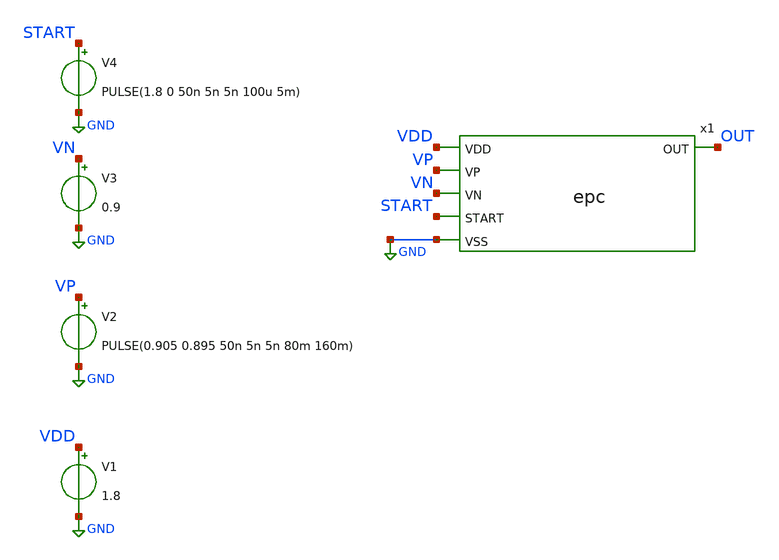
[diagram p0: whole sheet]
** sch_path: xschem/epc_tb.sch
**.subckt epc_tb
x1 VDD VP OUT VN START GND epc
V1 VDD GND 1.8
V2 VP GND PULSE(0.905 0.895 50n 5n 5n 80m 160m)
V3 VN GND 0.9
V4 START GND PULSE(1.8 0 50n 5n 5n 100u 5m)
**** begin user architecture code

** opencircuitdesign pdks install
.lib $::SKYWATER_MODELS/sky130.lib.spice tt
.include /usr/local/share/pdk/sky130A/libs.ref/sky130_fd_sc_hd/spice/sky130_fd_sc_hd.spice



.option wnflag=0
.option savecurrents
.control
tran 1m 640m
plot V(out)
plot V(vp) V(vn)
.endc

**** end user architecture code
**.ends
.GLOBAL GND
.end
